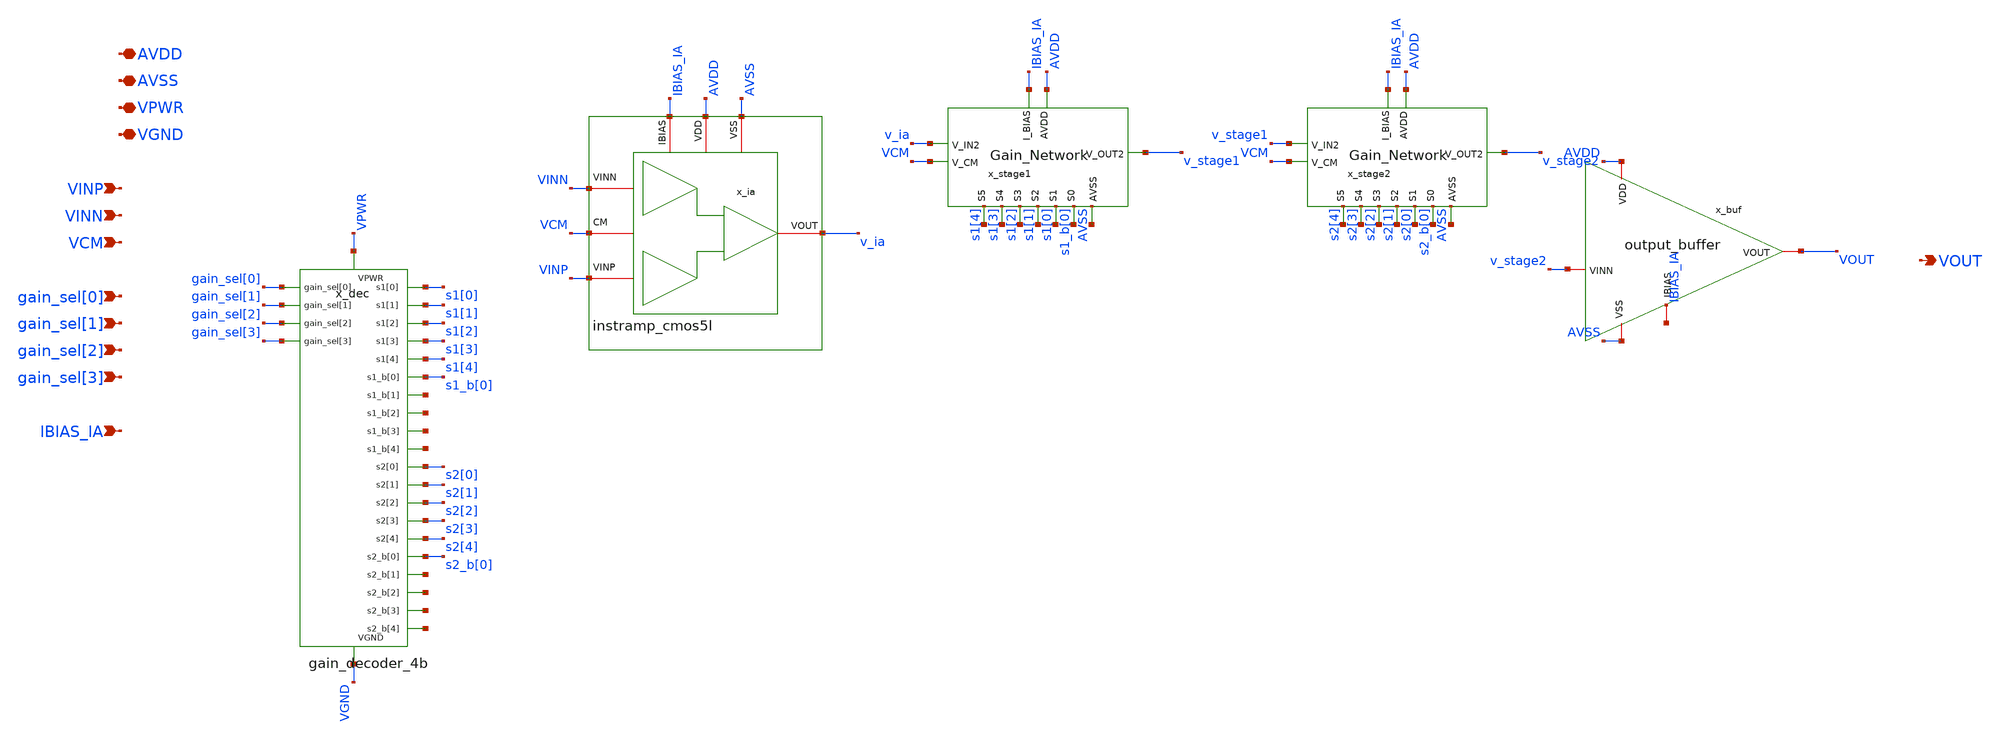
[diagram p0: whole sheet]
** sch_path: xschem/pgia_top/pgia_top.sch
**.subckt pgia_top AVDD AVSS VPWR VGND VINP VINN VCM gain_sel[0] gain_sel[1] gain_sel[2] gain_sel[3]
*+ IBIAS_IA VOUT
*.iopin AVDD
*.iopin AVSS
*.iopin VPWR
*.iopin VGND
*.ipin VINP
*.ipin VINN
*.ipin VCM
*.ipin gain_sel[0]
*.ipin gain_sel[1]
*.ipin gain_sel[2]
*.ipin gain_sel[3]
*.ipin IBIAS_IA
*.opin VOUT
x_dec VGND VPWR gain_sel[0] gain_sel[1] gain_sel[2] gain_sel[3] s1[0] s1[1] s1[2] s1[3] s1[4]
+ s1_b[0] net1 net2 net3 net4 s2[0] s2[1] s2[2] s2[3] s2[4] s2_b[0] net5 net6 net7 net8 gain_decoder_4b
x_ia AVSS AVDD IBIAS_IA VINN v_ia VINP VCM instramp_cmos5l
x_stage1 s1[3] s1[4] s1_b[0] s1[1] s1[0] s1[2] AVDD VCM v_ia v_stage1 IBIAS_IA AVSS gain_network
x_stage2 s2[3] s2[4] s2_b[0] s2[1] s2[0] s2[2] AVDD VCM v_stage1 v_stage2 IBIAS_IA AVSS gain_network
x_buf AVDD AVSS IBIAS_IA v_stage2 VOUT output_buffer
**.ends
.end
